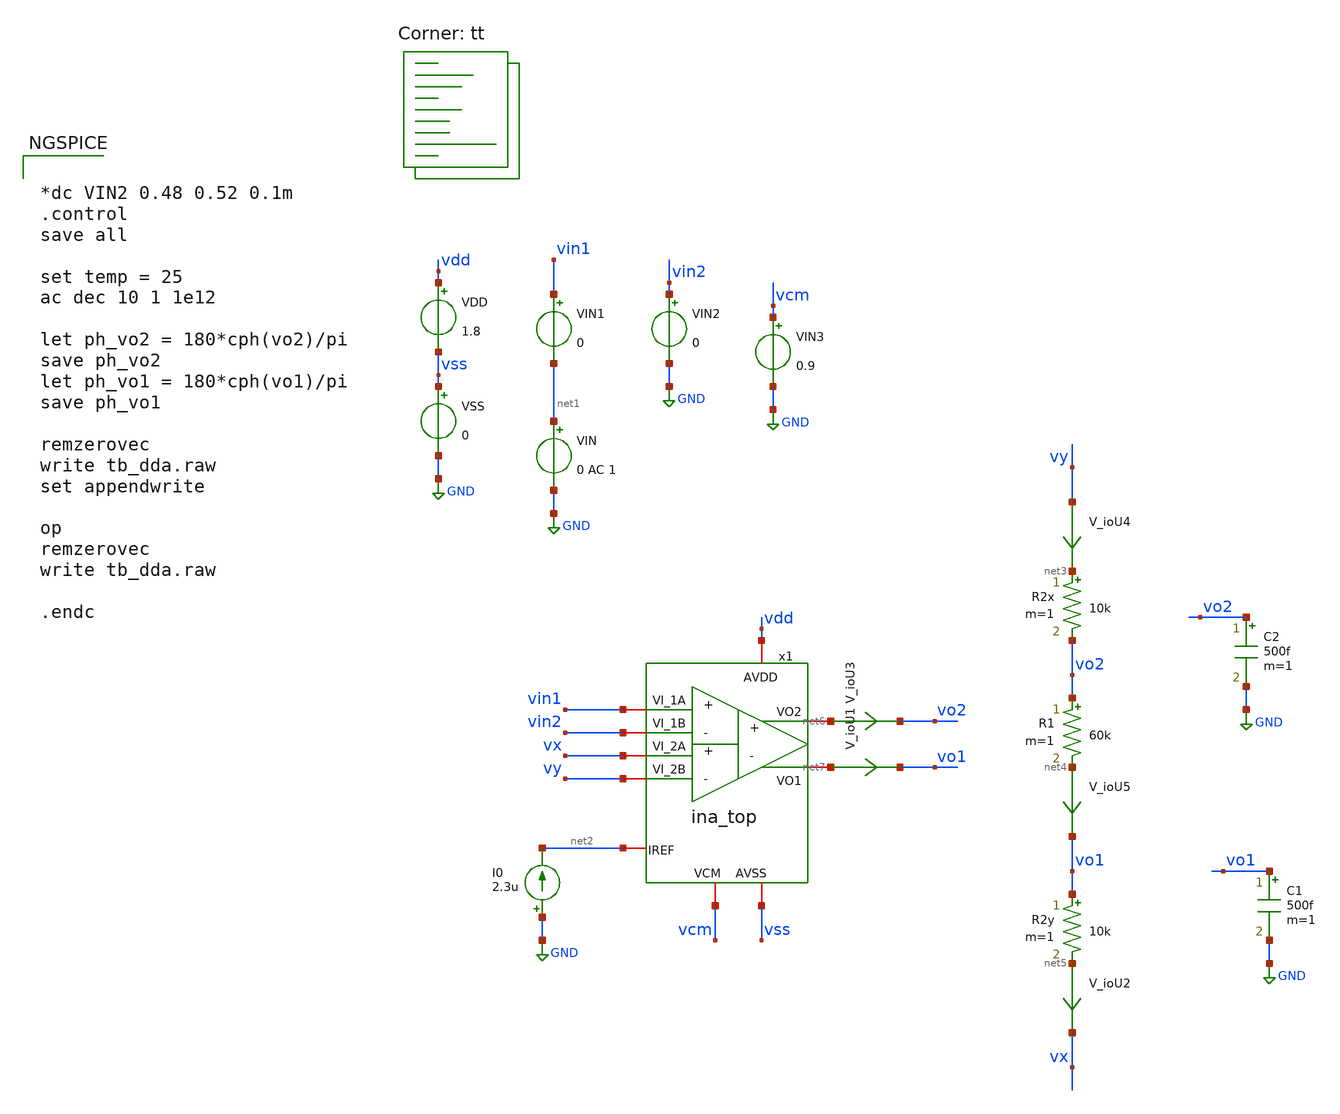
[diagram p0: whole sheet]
** sch_path: testbenches/tb_dda.sch
**.subckt tb_dda
VDD vdd vss 1.8
VSS vss GND 0
C1 vo1 GND 500f m=1
I0 GND net2 2.3u
VIN1 vin1 net1 0
VIN2 vin2 GND 0
VIN net1 GND 0 AC 1
C2 vo2 GND 500f m=1
VIN3 vcm GND 0.9
R2x net3 vo2 10k m=1
R1 vo2 net4 60k m=1
R2y vo1 net5 10k m=1
V_ioU3 net6 vo2 0
.save i(v_iou3)
V_ioU1 net7 vo1 0
.save i(v_iou1)
V_ioU2 net5 vx 0
.save i(v_iou2)
V_ioU4 vy net3 0
.save i(v_iou4)
V_ioU5 net4 vo1 0
.save i(v_iou5)
x1 vdd vss vin1 vin2 net6 net7 vcm net2 vx vy ina_top
**** begin user architecture code


*dc VIN2 0.48 0.52 0.1m
.control
save all

set temp = 25
ac dec 10 1 1e12

let ph_vo2 = 180*cph(vo2)/pi
save ph_vo2
let ph_vo1 = 180*cph(vo1)/pi
save ph_vo1

remzerovec
write tb_dda.raw
set appendwrite

op
remzerovec
write tb_dda.raw

.endc


.lib $::SKYWATER_MODELS/sky130.lib.spice tt
**** end user architecture code
**.ends
.GLOBAL GND
.end
